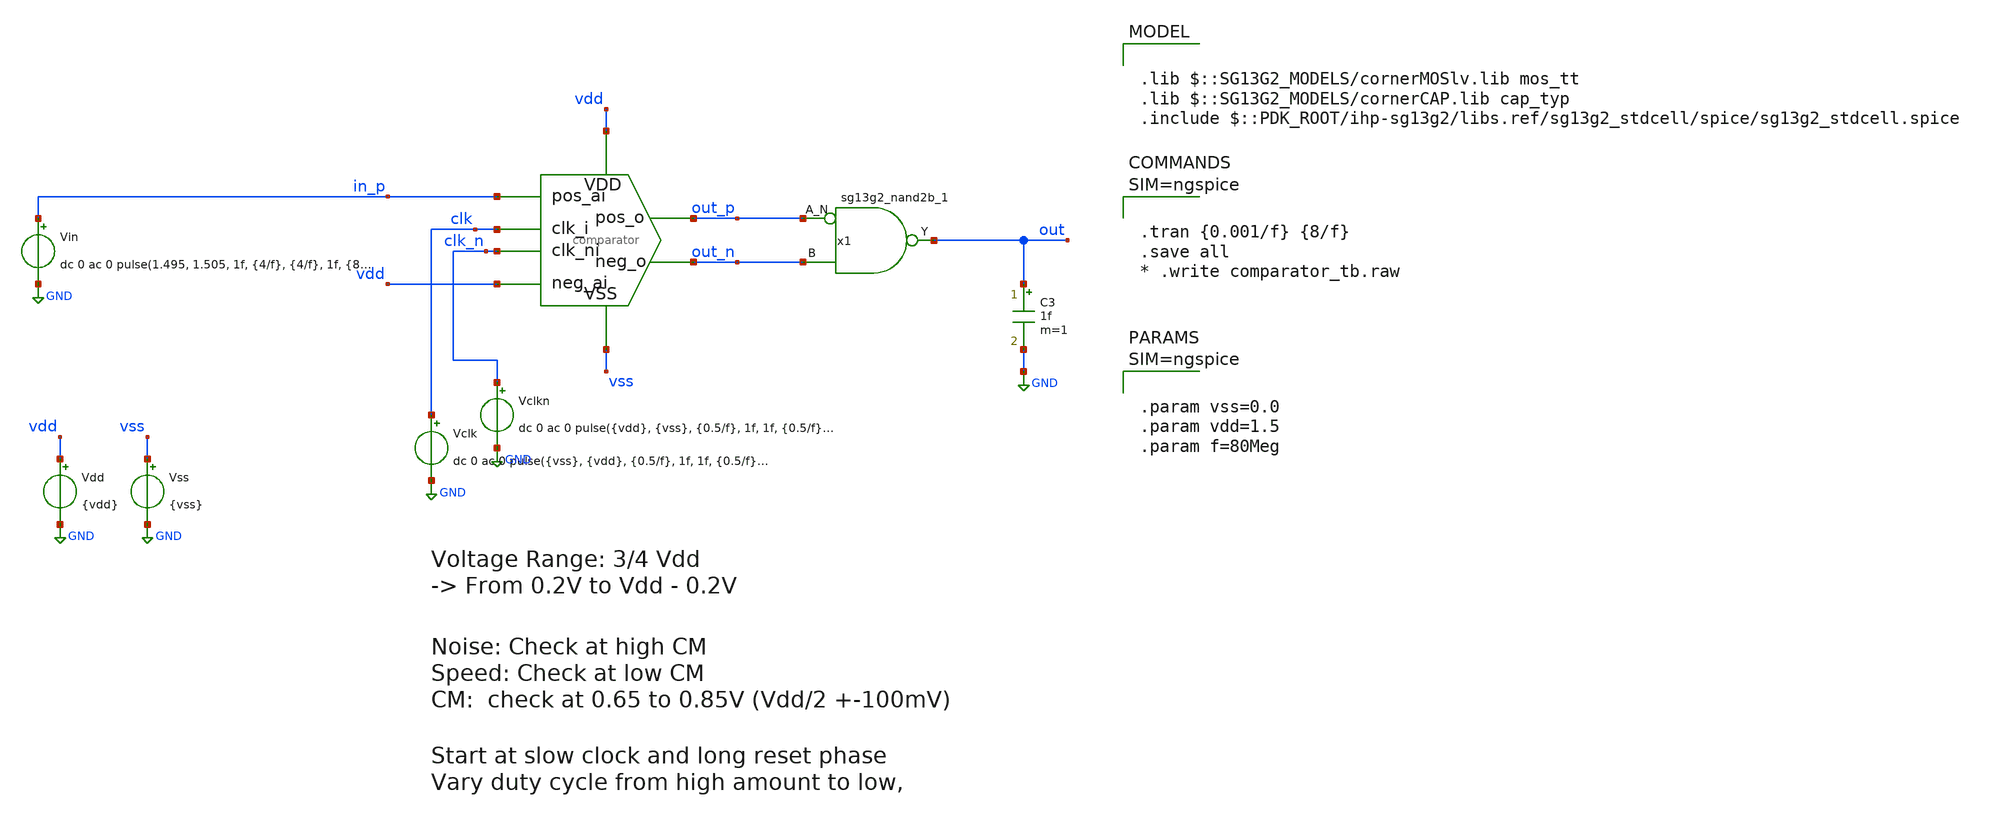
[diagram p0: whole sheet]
** sch_path: designs/comparator_dt/comparator_tb.sch
* IHP-GmbH/IHP-Open-PDK/ihp-sg13g2/libs.tech/xschem/sg13g2_stdcells/sg13g2_nand2b_1.sch:
* Copyright 2023 IHP PDK Authors
* Licensed under the Apache License, Version 2.0 (the "License");
**.subckt comparator_tb
x1 clk in_p vdd out_n out_p vss vdd clk_n comparator
Vdd vdd GND {vdd}
Vss vss GND {vss}
Vclk clk GND dc 0 ac 0 pulse({vss}, {vdd}, {0.5/f}, 1f, 1f, {0.5/f}, {1/f})
Vin in_p GND dc 0 ac 0 pulse(1.495, 1.505, 1f, {4/f}, {4/f}, 1f, {8/f})
C3 out GND 1f m=1
Vclkn clk_n GND dc 0 ac 0 pulse({vdd}, {vss}, {0.5/f}, 1f, 1f, {0.5/f}, {1/f})
x1 out out_p out_n VDD VSS sg13g2_nand2b_1
**** begin user architecture code

.lib $::SG13G2_MODELS/cornerMOSlv.lib mos_tt
.lib $::SG13G2_MODELS/cornerCAP.lib cap_typ
.include $::PDK_ROOT/ihp-sg13g2/libs.ref/sg13g2_stdcell/spice/sg13g2_stdcell.spice




.tran {0.001/f} {8/f}
.save all
* .write comparator_tb.raw






.param vss=0.0
.param vdd=1.5
.param f=80Meg



**** end user architecture code
**.ends

* expanding   symbol:  comparator.sym # of pins=8
** sym_path: designs/comparator_dt/comparator.sym
** sch_path: designs/comparator_dt/comparator.sch
.subckt comparator clk_i pos_ai neg_ai neg_o pos_o VSS VDD clk_ni
*.ipin pos_ai
*.ipin neg_ai
*.ipin VSS
*.ipin VDD
*.opin neg_o
*.opin pos_o
*.ipin clk_i
*.ipin clk_ni
XM12 neg_buf clk_i VDD VDD sg13_lv_pmos w=1.0u l=0.13u ng=1 m=1 mm_ok=1
XM13 pos_buf clk_i VDD VDD sg13_lv_pmos w=1.0u l=0.13u ng=1 m=1 mm_ok=1
XM14 net1 pos_ai neg_buf VSS sg13_lv_nmos w=1.0u l=0.13u ng=1 m=1 mm_ok=1
XM15 net1 neg_ai pos_buf VSS sg13_lv_nmos w=1.0u l=0.13u ng=1 m=1 mm_ok=1
XM16 VSS clk_i net1 VSS sg13_lv_nmos w=1.0u l=0.13u ng=1 m=1 mm_ok=1
XM17 net2 clk_ni VDD VDD sg13_lv_pmos w=2.0u l=0.13u ng=2 m=1 mm_ok=1
XM18 pos_o neg_o net2 VDD sg13_lv_pmos w=2.0u l=0.13u ng=2 m=1 mm_ok=1
XM19 neg_o pos_o net2 VDD sg13_lv_pmos w=2.0u l=0.13u ng=2 m=1 mm_ok=1
XM20 VSS neg_buf pos_o VSS sg13_lv_nmos w=1.0u l=0.13u ng=1 m=1 mm_ok=1
XM21 VSS neg_o pos_o VSS sg13_lv_nmos w=1.0u l=0.13u ng=1 m=1 mm_ok=1
XM22 VSS pos_o neg_o VSS sg13_lv_nmos w=1.0u l=0.13u ng=1 m=1 mm_ok=1
XM23 VSS pos_buf neg_o VSS sg13_lv_nmos w=1.0u l=0.13u ng=1 m=1 mm_ok=1
XC1 neg_buf VSS cap_cmim w=1.41e-5 l=1.41e-5 m=1 mm_ok=1
XC2 pos_buf VSS cap_cmim w=1.41e-5 l=1.41e-5 m=1 mm_ok=1
.ends


* expanding   symbol:  sg13g2_stdcells/sg13g2_nand2b_1.sym # of pins=3
** sym_path: sg13g2_stdcells/sg13g2_nand2b_1.sym
** sch_path: sg13g2_stdcells/sg13g2_nand2b_1.sch
.subckt sg13g2_nand2b_1 Y A_N B VDD VSS
*.opin Y
*.ipin B
*.ipin A_N
*.iopin VDD
*.iopin VSS
XM1 net1 A_N VSS VSS sg13_lv_nmos w=550.00n l=130.00n ng=1 m=1 mm_ok=1
XM2 Y net1 net2 VSS sg13_lv_nmos w=740.00n l=130.00n ng=1 m=1 mm_ok=1
XM3 net2 B VSS VSS sg13_lv_nmos w=740.00n l=130.00n ng=1 m=1 mm_ok=1
XM4 Y B VDD VDD sg13_lv_pmos w=1.12u l=130.00n ng=1 m=1 mm_ok=1
XM5 net1 A_N VDD VDD sg13_lv_pmos w=840.00n l=130.00n ng=1 m=1 mm_ok=1
XM6 Y net1 VDD VDD sg13_lv_pmos w=1.12u l=130.00n ng=1 m=1 mm_ok=1
.ends

.GLOBAL GND
.end
